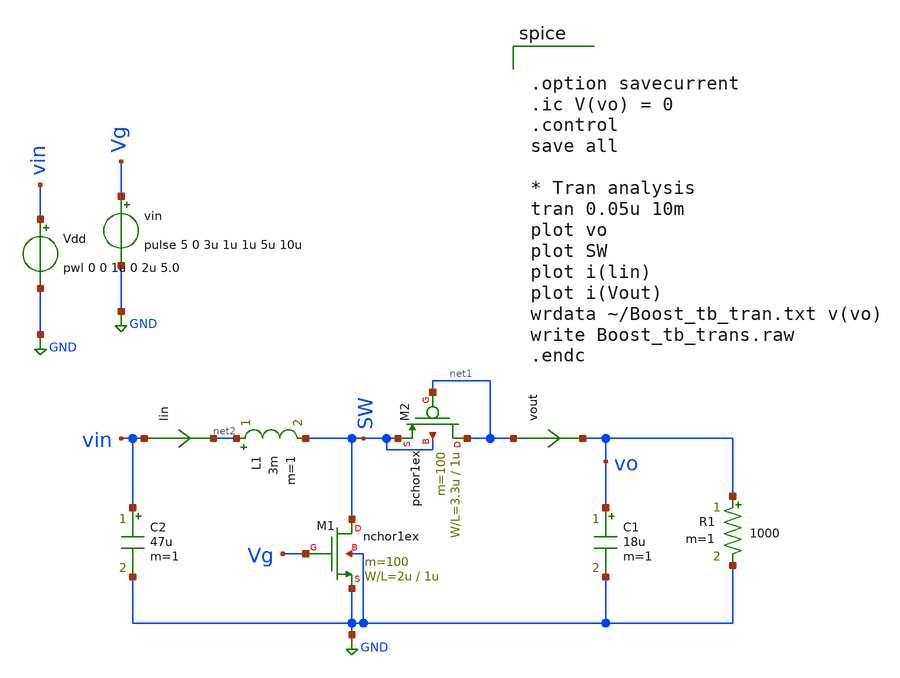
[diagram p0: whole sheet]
** sch_path: design/xschem/sebasu/BoostDCDC.sch
**.subckt BoostDCDC
M1 SW Vg GND GND nchor1ex L=1u W=2u m=100
L1 net2 SW 3m m=1
C1 vo GND 18u m=1
Vdd vin GND pwl 0 0 1u 0 2u 5.0
vin Vg GND pulse 5 0 3u 1u 1u 5u 10u
lin vin net2 0
.save i(lin)
M2 net1 net1 SW SW pchor1ex L=1u W=3.3u m=100
R1 vo GND 1000 m=1
vout net1 vo 0
.save i(vout)
C2 vin GND 47u m=1
**** begin user architecture code


.option savecurrent
.ic V(vo) = 0
.control
save all

* Tran analysis
tran 0.05u 10m
plot vo
plot SW
plot i(lin)
plot i(Vout)
wrdata ~/Boost_tb_tran.txt v(vo)
write Boost_tb_trans.raw
.endc

 .include $::LIB/mos.lib
.include $::LIB/passive.lib
.include $::LIB/diode.lib
**** end user architecture code
**.ends
.GLOBAL GND
.end
